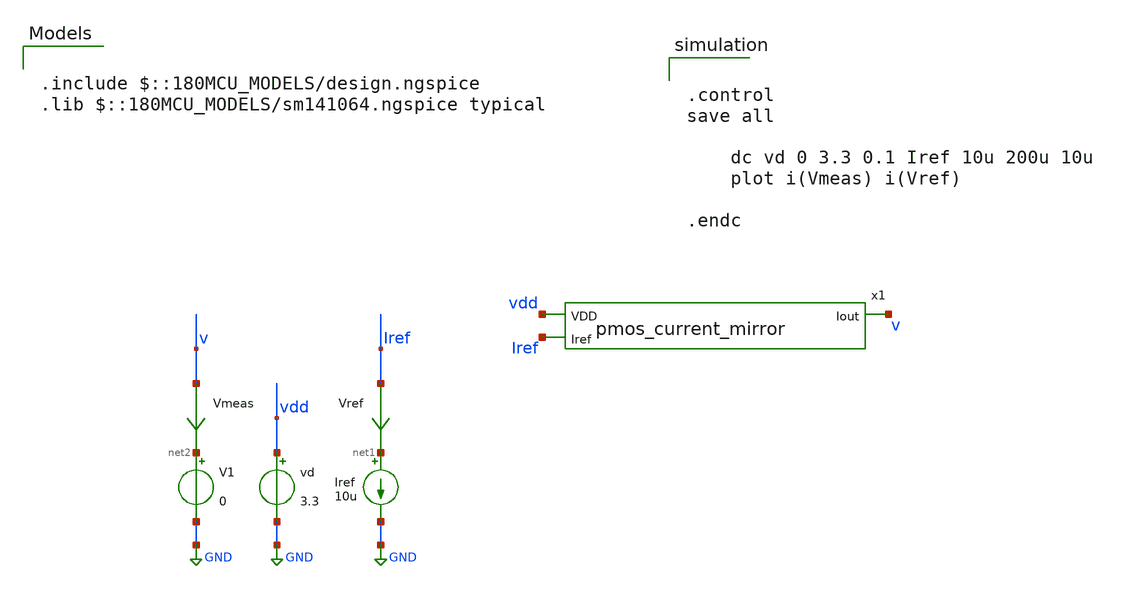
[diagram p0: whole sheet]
** sch_path: designs/libs/tb_current-mirror/tb_pmos_current_mirror/tb_pmos_current_mirror.sch
**.subckt tb_pmos_current_mirror
Iref net1 GND 10u
vd vdd GND 3.3
V1 net2 GND 0
Vmeas v net2 0
.save i(vmeas)
Vref Iref net1 0
.save i(vref)
x1 vdd v Iref pmos_current_mirror
**** begin user architecture code


.control
save all

	dc vd 0 3.3 0.1 Iref 10u 200u 10u
	plot i(Vmeas) i(Vref)

.endc



.include $::180MCU_MODELS/design.ngspice
.lib $::180MCU_MODELS/sm141064.ngspice typical

**** end user architecture code
**.ends
.GLOBAL GND
.end
